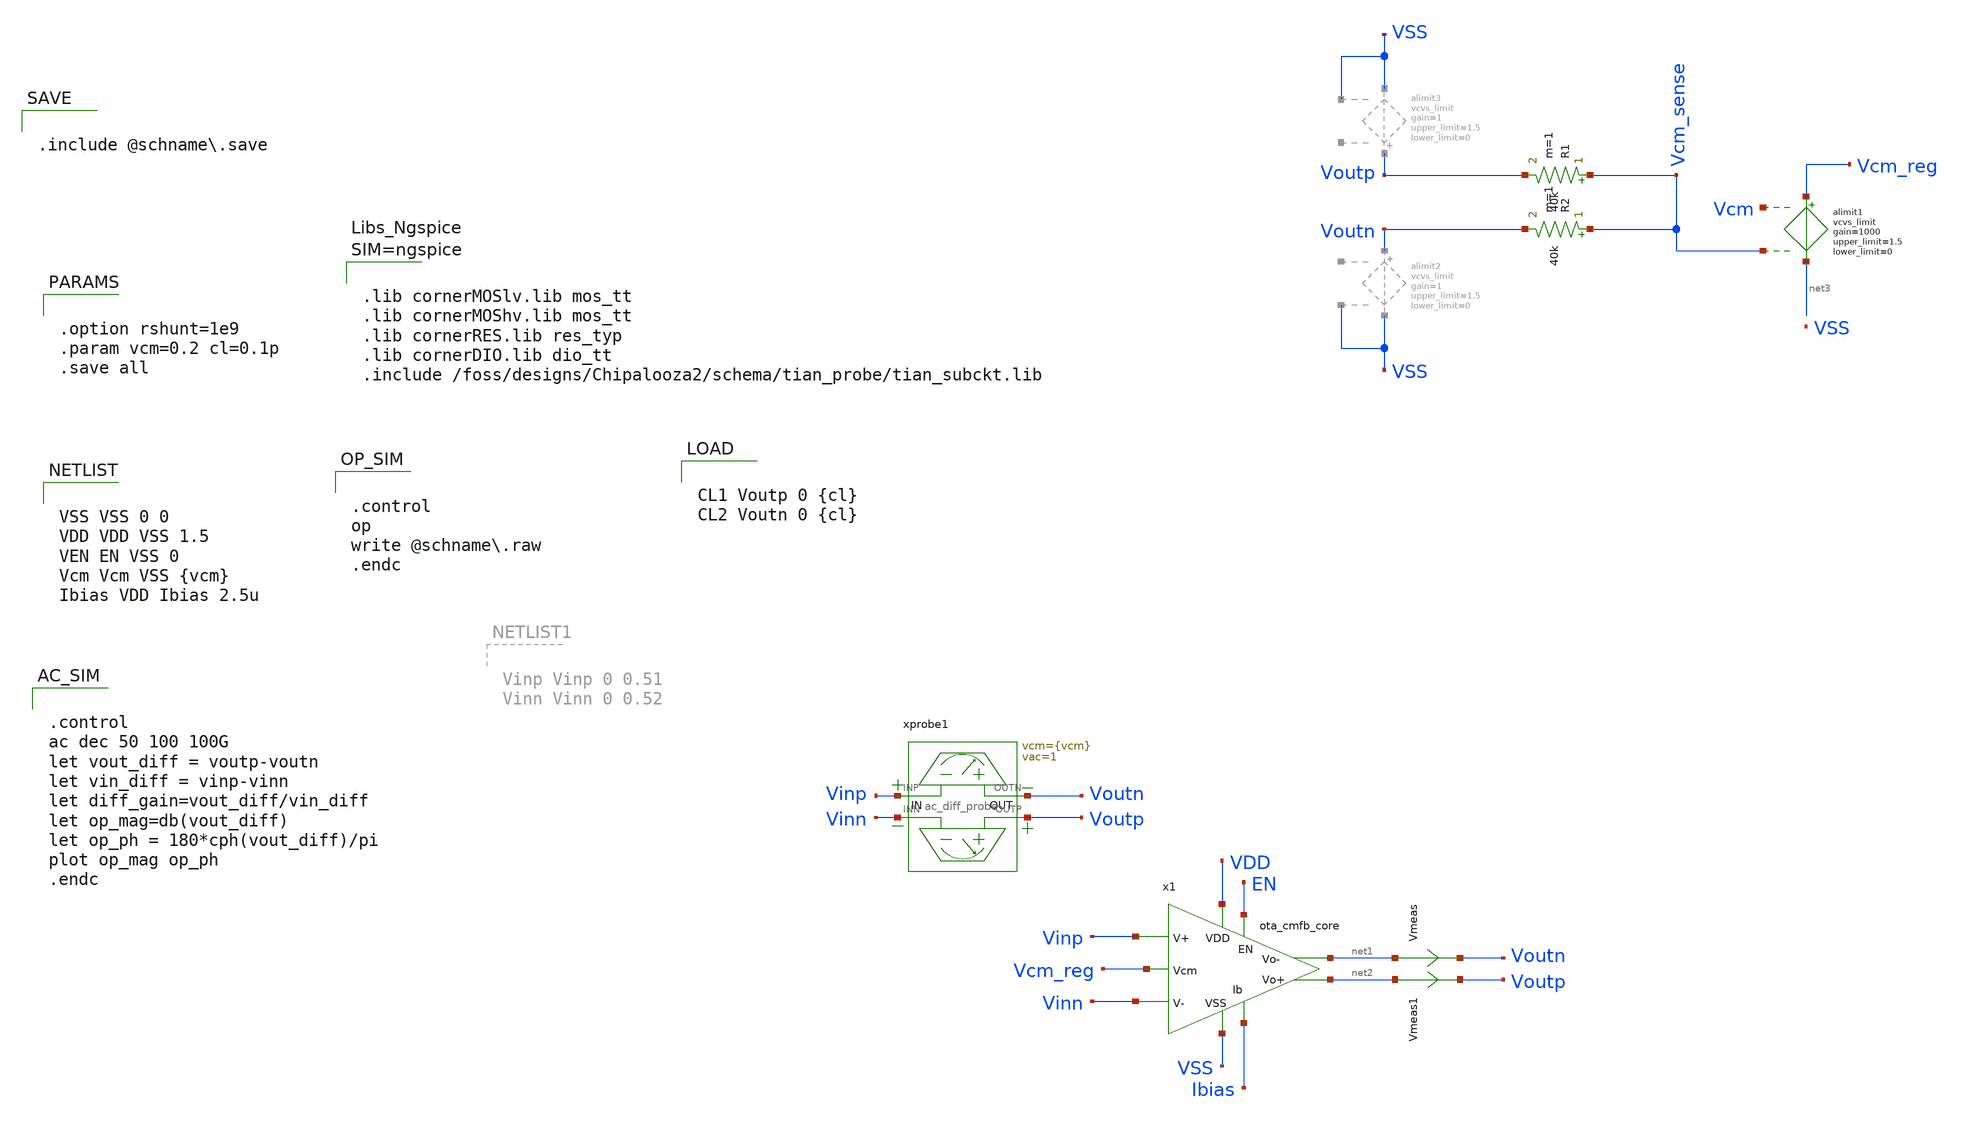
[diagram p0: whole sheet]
** sch_path: schema/ota_cmfb_core/ota_cmfb_core_tb.sch
**.subckt ota_cmfb_core_tb
x1 VDD Vcm_reg Vinn Vinp Ibias net1 net2 VSS EN ota_cmfb_core
alimit1 %vd( Vcm Vcm_sense ) %vd( Vcm_reg net3 ) alimit1
.model alimit1 limit ( gain=1000 out_lower_limit=0 out_upper_limit=1.5 )
xprobe1 Vinp Voutn Vinn Voutp ac_diff_probe vcm={vcm} vac=1
R1 Vcm_sense Voutp 40k m=1
R2 Vcm_sense Voutn 40k m=1
Vmeas net1 Voutn 0
.save i(vmeas)
Vmeas1 net2 Voutp 0
.save i(vmeas1)
**** begin user architecture code


VSS VSS 0 0
VDD VDD VSS 1.5
VEN EN VSS 0
Vcm Vcm VSS {vcm}
Ibias VDD Ibias 2.5u



.control
op
write @schname.raw
.endc




.lib cornerMOSlv.lib mos_tt
.lib cornerMOShv.lib mos_tt
.lib cornerRES.lib res_typ
.lib cornerDIO.lib dio_tt
.include /foss/designs/Chipalooza2/schema/tian_probe/tian_subckt.lib





.control
ac dec 50 100 100G
let vout_diff = voutp-voutn
let vin_diff = vinp-vinn
let diff_gain=vout_diff/vin_diff
let op_mag=db(vout_diff)
let op_ph = 180*cph(vout_diff)/pi
plot op_mag op_ph
.endc




.option rshunt=1e9
.param vcm=0.2 cl=0.1p
.save all




CL1 Voutp 0 {cl}
CL2 Voutn 0 {cl}



.include @schname.save

**** end user architecture code
**.ends

* expanding   symbol:  /foss/designs/Chipalooza2/schema/ota_cmfb_core/ota_cmfb_core.sym # of pins=9
** sym_path: schema/ota_cmfb_core/ota_cmfb_core.sym
** sch_path: schema/ota_cmfb_core/ota_cmfb_core.sch
.subckt ota_cmfb_core VDD Vcm_reg Vinn Vinp Ibias Voutn Voutp VSS EN
*.opin Voutn
*.opin Voutp
*.iopin VDD
*.iopin VSS
*.ipin Vinp
*.ipin Ibias
*.ipin Vinn
*.ipin Vcm_reg
*.ipin EN
XM1 Voutp_st1 Ibias VSS VSS sg13_lv_nmos w=0.5u l=10u ng=1 m=4 mm_ok=1
XM2 net1 Vinn Voutp_st1 VDD sg13_lv_pmos w=2.5u l=2u ng=1 m=8 mm_ok=1
XM3 Voutn_st1 Ibias VSS VSS sg13_lv_nmos w=0.5u l=10u ng=1 m=4 mm_ok=1
XM4 net1 Vinp Voutn_st1 VDD sg13_lv_pmos w=2.5u l=2u ng=1 m=8 mm_ok=1
XM5 VDD Vcm_reg net1 VDD sg13_lv_pmos w=5u l=10u ng=1 m=4 mm_ok=1
XM6 Ibias Ibias VSS VSS sg13_lv_nmos w=0.5u l=10u ng=1 m=1 mm_ok=1
XM7 Ibias EN VSS VSS sg13_lv_nmos w=0.15u l=0.13u ng=1 m=1 mm_ok=1
xsf1 VDD net2 Voutp Ibias VSS ota_cmfb_core_push_pull_output_stage
xsf2 VDD net3 Voutn Ibias VSS ota_cmfb_core_push_pull_output_stage
Vmeas Voutn_st1 net2 0
.save i(vmeas)
Vmeas1 Voutp_st1 net3 0
.save i(vmeas1)
.ends


* expanding   symbol:  /foss/designs/Chipalooza2/schema/ac_diff_probe/ac_diff_probe.sym # of pins=4
** sym_path: schema/ac_diff_probe/ac_diff_probe.sym
** sch_path: schema/ac_diff_probe/ac_diff_probe.sch
.subckt ac_diff_probe INP OUTN INN OUTP  vcm=0.75 vac=0.1
*.iopin OUTN
*.iopin INP
*.iopin OUTP
*.iopin INN
xprobe1 OUTN INP ac_probe vcm={vcm} vac={vac}
xprobe2 OUTP INN ac_probe vcm={vcm} vac=-{vac}
.ends


* expanding   symbol:
*+  /foss/designs/Chipalooza2/schema/ota_cmfb_core/ota_cmfb_core_push_pull_output_stage.sym # of pins=5
** sym_path: schema/ota_cmfb_core/ota_cmfb_core_push_pull_output_stage.sym
** sch_path: schema/ota_cmfb_core/ota_cmfb_core_push_pull_output_stage.sch
.subckt ota_cmfb_core_push_pull_output_stage VDD Vin Vout Vbias VSS
*.iopin VSS
*.iopin VDD
*.ipin Vbias
*.ipin Vin
*.opin Vout
XM1 Vout Vin_shifted VSS VSS sg13_lv_nmos w=2.5u l=0.5u ng=1 m=2 mm_ok=1
XM2 VDD Vin Vout VDD sg13_lv_pmos w=5u l=0.5u ng=1 m=4 mm_ok=1
XM5 VDD Vbiasp net2 VDD sg13_lv_pmos w=10u l=3u ng=1 m=1 mm_ok=1
XM6 net1 Vbiasn VSS VSS sg13_lv_nmos w=5u l=0.5u ng=1 m=1 mm_ok=1
XM4 Vin_shifted Vcasp2 Vin VDD sg13_lv_pmos w=5u l=3u ng=1 m=1 mm_ok=1
XM15 Vin_shifted Vcasn net1 VSS sg13_lv_nmos w=5u l=0.5u ng=1 m=1 mm_ok=1
XM16 net2 Vcasp Vin VDD sg13_lv_pmos w=10u l=3u ng=1 m=1 mm_ok=1
XM3 Vin Vcasn2 Vin_shifted VSS sg13_lv_nmos w=1.4u l=3u ng=1 m=1 mm_ok=1
XM8 VDD Vbiasp Vbiasp VDD sg13_lv_pmos w=10u l=3u ng=1 m=1 mm_ok=1
XM9 Vbiasp Vcasp Vcasp VDD sg13_lv_pmos w=10u l=3u ng=1 m=1 mm_ok=1
XM13 Vcasp Vcasp2 Vcasp2 VDD sg13_lv_pmos w=5u l=3u ng=1 m=2 mm_ok=1
XM10 VDD Vbiasp Vcasn2 VDD sg13_lv_pmos w=10u l=3u ng=1 m=1 mm_ok=1
XM11 Vcasn2 Vcasn2 Vcasn VSS sg13_lv_nmos w=1.4u l=3u ng=1 m=2 mm_ok=1
XM12 Vcasn Vcasn Vbiasn VSS sg13_lv_nmos w=5u l=0.5u ng=1 m=1 mm_ok=1
XM14 Vbiasn Vbiasn VSS VSS sg13_lv_nmos w=5u l=0.5u ng=1 m=1 mm_ok=1
XM7 Vcasp2 Vbias VSS VSS sg13_lv_nmos w=2u l=1u ng=1 m=2 mm_ok=1
.ends


* expanding   symbol:  ac_probe/ac_probe.sym # of pins=2
** sym_path: schema/ac_probe/ac_probe.sym
** sch_path: schema/ac_probe/ac_probe.sch
.subckt ac_probe OUT IN  vcm=0.75 vac=0.01

*.iopin IN
*.iopin OUT
C1 net1 IN 1 m=1
V1 net1 0 {vcm} ac {vac}
L1 OUT IN 1G m=1
.ends

.end
